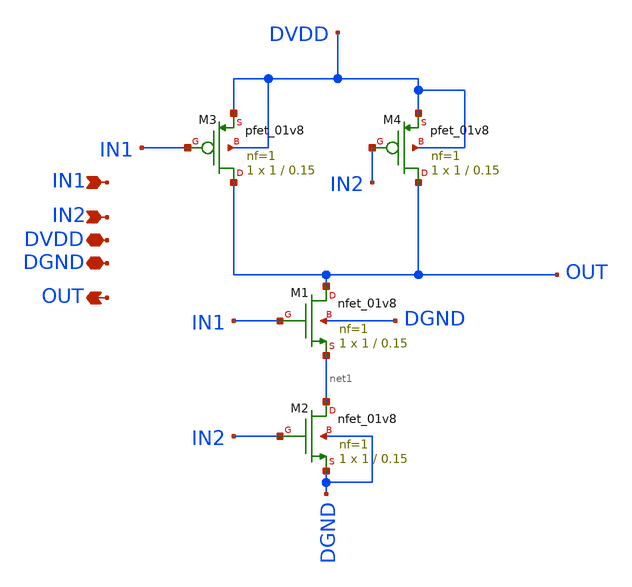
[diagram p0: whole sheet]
** sch_path: xschem/NAND2/NAND2_eymenunay.sch
**.subckt NAND2_eymenunay IN1 IN2 OUT DVDD DGND
*.ipin IN1
*.ipin IN2
*.opin OUT
*.iopin DVDD
*.iopin DGND
XM1 OUT IN1 net1 DGND sky130_fd_pr__nfet_01v8 L=0.15 W=1 nf=1 ad='int((nf+1)/2) * W/nf * 0.29' as='int((nf+2)/2) * W/nf * 0.29'
+ pd='2*int((nf+1)/2) * (W/nf + 0.29)' ps='2*int((nf+2)/2) * (W/nf + 0.29)' nrd='0.29 / W' nrs='0.29 / W'
+ sa=0 sb=0 sd=0 mult=1 m=1
XM2 net1 IN2 DGND DGND sky130_fd_pr__nfet_01v8 L=0.15 W=1 nf=1 ad='int((nf+1)/2) * W/nf * 0.29' as='int((nf+2)/2) * W/nf * 0.29'
+ pd='2*int((nf+1)/2) * (W/nf + 0.29)' ps='2*int((nf+2)/2) * (W/nf + 0.29)' nrd='0.29 / W' nrs='0.29 / W'
+ sa=0 sb=0 sd=0 mult=1 m=1
XM3 OUT IN1 DVDD DVDD sky130_fd_pr__pfet_01v8 L=0.15 W=1 nf=1 ad='int((nf+1)/2) * W/nf * 0.29' as='int((nf+2)/2) * W/nf * 0.29'
+ pd='2*int((nf+1)/2) * (W/nf + 0.29)' ps='2*int((nf+2)/2) * (W/nf + 0.29)' nrd='0.29 / W' nrs='0.29 / W'
+ sa=0 sb=0 sd=0 mult=1 m=1
XM4 OUT IN2 DVDD DVDD sky130_fd_pr__pfet_01v8 L=0.15 W=1 nf=1 ad='int((nf+1)/2) * W/nf * 0.29' as='int((nf+2)/2) * W/nf * 0.29'
+ pd='2*int((nf+1)/2) * (W/nf + 0.29)' ps='2*int((nf+2)/2) * (W/nf + 0.29)' nrd='0.29 / W' nrs='0.29 / W'
+ sa=0 sb=0 sd=0 mult=1 m=1
**.ends
.end
